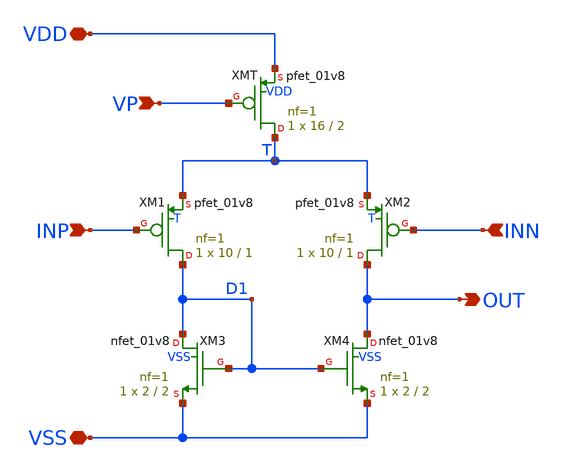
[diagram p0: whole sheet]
** sch_path: xschem/ota5p.sch
**.subckt ota5p INP INN VP OUT VDD VSS
*.ipin INP
*.ipin INN
*.ipin VP
*.opin OUT
*.iopin VDD
*.iopin VSS
XXM1 D1 INP T T sky130_fd_pr__pfet_01v8 L=1 W=10 nf=1 ad='int((1 + 1)/2) * 10 / 1 * 0.29' as='int((1 + 2)/2) * 10 / 1 * 0.29'
+ pd='2*int((1 + 1)/2) * (10 / 1 + 0.29)' ps='2*int((1 + 2)/2) * (10 / 1 + 0.29)' nrd='0.29 / 10 ' nrs='0.29 / 10 '
+ sa=0 sb=0 sd=0 mult=1 m=1
XXM2 OUT INN T T sky130_fd_pr__pfet_01v8 L=1 W=10 nf=1 ad='int((1 + 1)/2) * 10 / 1 * 0.29' as='int((1 + 2)/2) * 10 / 1 * 0.29'
+ pd='2*int((1 + 1)/2) * (10 / 1 + 0.29)' ps='2*int((1 + 2)/2) * (10 / 1 + 0.29)' nrd='0.29 / 10 ' nrs='0.29 / 10 '
+ sa=0 sb=0 sd=0 mult=1 m=1
XXMT T VP VDD VDD sky130_fd_pr__pfet_01v8 L=2 W=16 nf=1 ad='int((1 + 1)/2) * 16 / 1 * 0.29' as='int((1 + 2)/2) * 16 / 1 * 0.29'
+ pd='2*int((1 + 1)/2) * (16 / 1 + 0.29)' ps='2*int((1 + 2)/2) * (16 / 1 + 0.29)' nrd='0.29 / 16 ' nrs='0.29 / 16 '
+ sa=0 sb=0 sd=0 mult=1 m=1
XXM3 D1 D1 VSS VSS sky130_fd_pr__nfet_01v8 L=2 W=2 nf=1 ad='int((nf+1)/2) * W/nf * 0.29' as='int((nf+2)/2) * W/nf * 0.29'
+ pd='2*int((nf+1)/2) * (W/nf + 0.29)' ps='2*int((nf+2)/2) * (W/nf + 0.29)' nrd='0.29 / W' nrs='0.29 / W'
+ sa=0 sb=0 sd=0 mult=1 m=1
XXM4 OUT D1 VSS VSS sky130_fd_pr__nfet_01v8 L=2 W=2 nf=1 ad='int((nf+1)/2) * W/nf * 0.29' as='int((nf+2)/2) * W/nf * 0.29'
+ pd='2*int((nf+1)/2) * (W/nf + 0.29)' ps='2*int((nf+2)/2) * (W/nf + 0.29)' nrd='0.29 / W' nrs='0.29 / W'
+ sa=0 sb=0 sd=0 mult=1 m=1
**.ends
.end
